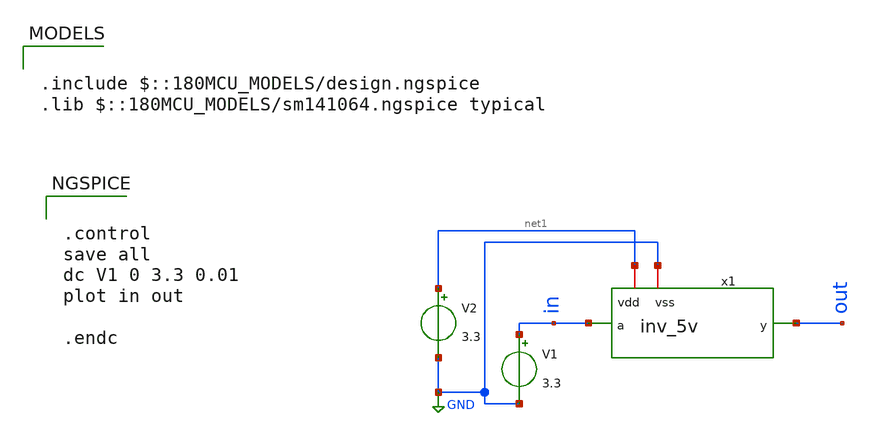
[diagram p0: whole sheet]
** sch_path: member_project/ice458/dynamic_comparator/xschem/inv_5v_tb.sch
**.subckt inv_5v_tb
V1 in GND 3.3
V2 net1 GND 3.3
x1 net1 in out GND inv_5v
**** begin user architecture code

.include $::180MCU_MODELS/design.ngspice
.lib $::180MCU_MODELS/sm141064.ngspice typical



.control
save all
dc V1 0 3.3 0.01
plot in out

.endc


**** end user architecture code
**.ends

* expanding   symbol:  inv_5v.sym # of pins=4
** sym_path: member_project/ice458/dynamic_comparator/xschem/inv_5v.sym
** sch_path: member_project/ice458/dynamic_comparator/xschem/inv_5v.sch
.subckt inv_5v vdd a y vss
*.iopin vdd
*.iopin vss
*.ipin a
*.opin y
XM3 y a vss vss nfet_06v0 L=0.70u W=1u nf=1 ad='int((nf+1)/2) * W/nf * 0.18u' as='int((nf+2)/2) * W/nf * 0.18u'
+ pd='2*int((nf+1)/2) * (W/nf + 0.18u)' ps='2*int((nf+2)/2) * (W/nf + 0.18u)' nrd='0.18u / W' nrs='0.18u / W'
+ sa=0 sb=0 sd=0 m=1
XM5 y a vdd vdd pfet_05v0 L=0.7u W=3u nf=1 ad='int((nf+1)/2) * W/nf * 0.18u' as='int((nf+2)/2) * W/nf * 0.18u'
+ pd='2*int((nf+1)/2) * (W/nf + 0.18u)' ps='2*int((nf+2)/2) * (W/nf + 0.18u)' nrd='0.18u / W' nrs='0.18u / W'
+ sa=0 sb=0 sd=0 m=1
.ends

.GLOBAL GND
.end
